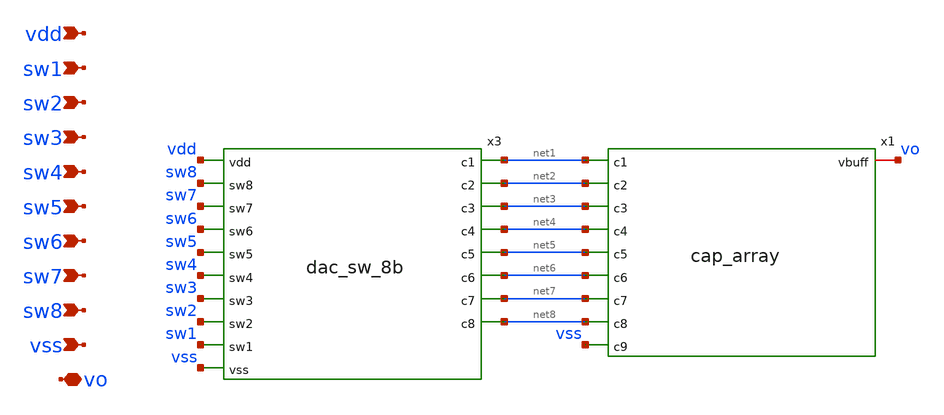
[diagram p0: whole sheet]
** sch_path: xschem/dac_8b.sch
**.subckt dac_8b vdd sw1 sw2 sw3 sw4 sw5 sw6 sw7 sw8 vss vo
*.ipin vdd
*.ipin sw1
*.ipin sw2
*.ipin sw3
*.ipin sw4
*.ipin sw5
*.ipin sw6
*.ipin sw7
*.ipin sw8
*.ipin vss
*.iopin vo
x1 net1 net2 net3 net4 net5 net6 net7 net8 vss vo cap_array
x3 vdd sw8 sw7 net1 net2 sw6 sw5 net3 sw4 net4 net5 sw3 net6 sw2 net7 sw1 net8 vss dac_sw_8b
**.ends

* expanding   symbol:  cap_array.sym # of pins=10
** sym_path: xschem/cap_array.sym
** sch_path: xschem/cap_array.sch
.subckt cap_array c1 c2 c3 c4 c5 c6 c7 c8 c9 vbuff
*.ipin c1
*.ipin c2
*.ipin c3
*.ipin c4
*.ipin c5
*.ipin c6
*.ipin c7
*.ipin c8
*.ipin c9
*.iopin vbuff
XC1 vbuff c9 sky130_fd_pr__cap_mim_m3_1 W=1 L=1 MF=1 m=1
XC2 vbuff c8 sky130_fd_pr__cap_mim_m3_1 W=1 L=1 MF=1 m=1
XC3 vbuff c7 sky130_fd_pr__cap_mim_m3_1 W=1 L=1 MF=2 m=2
XC4 vbuff c6 sky130_fd_pr__cap_mim_m3_1 W=1 L=1 MF=4 m=4
XC5 vbuff c5 sky130_fd_pr__cap_mim_m3_1 W=1 L=1 MF=8 m=8
XC6 vbuff c4 sky130_fd_pr__cap_mim_m3_1 W=1 L=1 MF=16 m=16
XC7 vbuff c3 sky130_fd_pr__cap_mim_m3_1 W=1 L=1 MF=32 m=32
XC8 vbuff c2 sky130_fd_pr__cap_mim_m3_1 W=1 L=1 MF=64 m=64
XC9 vbuff c1 sky130_fd_pr__cap_mim_m3_1 W=1 L=1 MF=128 m=128
.ends


* expanding   symbol:  dac_sw_8b.sym # of pins=18
** sym_path: xschem/dac_sw_8b.sym
** sch_path: xschem/dac_sw_8b.sch
.subckt dac_sw_8b vdd sw8 sw7 c1 c2 sw6 sw5 c3 sw4 c4 c5 sw3 c6 sw2 c7 sw1 c8 vss
*.ipin vdd
*.ipin sw8
*.ipin sw7
*.ipin sw6
*.ipin sw5
*.ipin sw4
*.ipin sw3
*.ipin sw2
*.ipin sw1
*.ipin vss
*.opin c8
*.opin c7
*.opin c6
*.opin c5
*.opin c4
*.opin c3
*.opin c2
*.opin c1
x1 net1 vss vss vdd vdd c8 sky130_fd_sc_hd__clkinv_16
x2 net2 vss vss vdd vdd c7 sky130_fd_sc_hd__clkinv_16
x3 net3 vss vss vdd vdd c6 sky130_fd_sc_hd__clkinv_16
x4 net4 vss vss vdd vdd c5 sky130_fd_sc_hd__clkinv_16
x5 net5 vss vss vdd vdd c4 sky130_fd_sc_hd__clkinv_16
x6 net6 vss vss vdd vdd c3 sky130_fd_sc_hd__clkinv_16
x7 net7 vss vss vdd vdd c2 sky130_fd_sc_hd__clkinv_16
x8 net8 vss vss vdd vdd c1 sky130_fd_sc_hd__clkinv_16
x9 sw8 vss vss vdd vdd net1 sky130_fd_sc_hd__inv_1
x10 sw7 vss vss vdd vdd net2 sky130_fd_sc_hd__inv_1
x11 sw6 vss vss vdd vdd net3 sky130_fd_sc_hd__inv_1
x12 sw5 vss vss vdd vdd net4 sky130_fd_sc_hd__inv_1
x13 sw4 vss vss vdd vdd net5 sky130_fd_sc_hd__inv_1
x14 sw3 vss vss vdd vdd net6 sky130_fd_sc_hd__inv_1
x15 sw2 vss vss vdd vdd net7 sky130_fd_sc_hd__inv_1
x16 sw1 vss vss vdd vdd net8 sky130_fd_sc_hd__inv_1
.ends

.end
